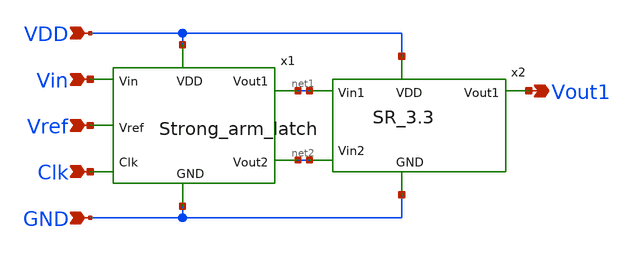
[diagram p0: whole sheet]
** sch_path: Comparator_Strong.sch
**.subckt Comparator_Strong Vin Vref Clk GND VDD Vout1
*.ipin Vin
*.ipin Vref
*.ipin Clk
*.ipin GND
*.ipin VDD
*.opin Vout1
x1 VDD net2 net1 Vin Vref Clk GND Strong_arm_latch
x2 net2 net1 VDD GND Vout1 SR_3.3
**.ends

* expanding   symbol:  /home/huydq/Strong_arm_latch.sym # of pins=7
** sym_path: Strong_arm_latch.sym
** sch_path: Strong_arm_latch.sch
.subckt Strong_arm_latch VDD Vout2 Vout1 Vin Vref Clk GND
*.ipin Vin
*.ipin Vref
*.ipin Clk
*.ipin VDD
*.opin Vout2
*.opin Vout1
*.ipin GND
XM8 Vout2 Vout1 net2 GND sky130_fd_pr__nfet_g5v0d10v5 L=0.5 W=8 nf=4 ad='int((nf+1)/2) * W/nf * 0.29'
+ as='int((nf+2)/2) * W/nf * 0.29' pd='2*int((nf+1)/2) * (W/nf + 0.29)' ps='2*int((nf+2)/2) * (W/nf + 0.29)'
+ nrd='0.29 / W' nrs='0.29 / W' sa=0 sb=0 sd=0 mult=1 m=1
XM7 Vout1 Vout2 net1 GND sky130_fd_pr__nfet_g5v0d10v5 L=0.5 W=8 nf=4 ad='int((nf+1)/2) * W/nf * 0.29'
+ as='int((nf+2)/2) * W/nf * 0.29' pd='2*int((nf+1)/2) * (W/nf + 0.29)' ps='2*int((nf+2)/2) * (W/nf + 0.29)'
+ nrd='0.29 / W' nrs='0.29 / W' sa=0 sb=0 sd=0 mult=1 m=1
XM10 Vout2 Vout1 VDD VDD sky130_fd_pr__pfet_g5v0d10v5 L=0.5 W=16 nf=8 ad='int((nf+1)/2) * W/nf * 0.29'
+ as='int((nf+2)/2) * W/nf * 0.29' pd='2*int((nf+1)/2) * (W/nf + 0.29)' ps='2*int((nf+2)/2) * (W/nf + 0.29)'
+ nrd='0.29 / W' nrs='0.29 / W' sa=0 sb=0 sd=0 mult=1 m=1
XM1 Vout1 Vout2 VDD VDD sky130_fd_pr__pfet_g5v0d10v5 L=0.5 W=16 nf=8 ad='int((nf+1)/2) * W/nf * 0.29'
+ as='int((nf+2)/2) * W/nf * 0.29' pd='2*int((nf+1)/2) * (W/nf + 0.29)' ps='2*int((nf+2)/2) * (W/nf + 0.29)'
+ nrd='0.29 / W' nrs='0.29 / W' sa=0 sb=0 sd=0 mult=1 m=1
XM2 net1 Clk VDD VDD sky130_fd_pr__pfet_g5v0d10v5 L=0.5 W=2 nf=2 ad='int((nf+1)/2) * W/nf * 0.29' as='int((nf+2)/2) * W/nf * 0.29'
+ pd='2*int((nf+1)/2) * (W/nf + 0.29)' ps='2*int((nf+2)/2) * (W/nf + 0.29)' nrd='0.29 / W' nrs='0.29 / W'
+ sa=0 sb=0 sd=0 mult=1 m=1
XM3 Vout1 Clk VDD VDD sky130_fd_pr__pfet_g5v0d10v5 L=0.5 W=2 nf=2 ad='int((nf+1)/2) * W/nf * 0.29' as='int((nf+2)/2) * W/nf * 0.29'
+ pd='2*int((nf+1)/2) * (W/nf + 0.29)' ps='2*int((nf+2)/2) * (W/nf + 0.29)' nrd='0.29 / W' nrs='0.29 / W'
+ sa=0 sb=0 sd=0 mult=1 m=1
XM4 Vout2 Clk VDD VDD sky130_fd_pr__pfet_g5v0d10v5 L=0.5 W=2 nf=2 ad='int((nf+1)/2) * W/nf * 0.29' as='int((nf+2)/2) * W/nf * 0.29'
+ pd='2*int((nf+1)/2) * (W/nf + 0.29)' ps='2*int((nf+2)/2) * (W/nf + 0.29)' nrd='0.29 / W' nrs='0.29 / W'
+ sa=0 sb=0 sd=0 mult=1 m=1
XM5 net2 Clk VDD VDD sky130_fd_pr__pfet_g5v0d10v5 L=0.5 W=2 nf=2 ad='int((nf+1)/2) * W/nf * 0.29' as='int((nf+2)/2) * W/nf * 0.29'
+ pd='2*int((nf+1)/2) * (W/nf + 0.29)' ps='2*int((nf+2)/2) * (W/nf + 0.29)' nrd='0.29 / W' nrs='0.29 / W'
+ sa=0 sb=0 sd=0 mult=1 m=1
XM6 net1 Vop GND GND sky130_fd_pr__nfet_g5v0d10v5 L=0.5 W=12 nf=6 ad='int((nf+1)/2) * W/nf * 0.29' as='int((nf+2)/2) * W/nf * 0.29'
+ pd='2*int((nf+1)/2) * (W/nf + 0.29)' ps='2*int((nf+2)/2) * (W/nf + 0.29)' nrd='0.29 / W' nrs='0.29 / W'
+ sa=0 sb=0 sd=0 mult=1 m=1
XM9 net2 Von GND GND sky130_fd_pr__nfet_g5v0d10v5 L=0.5 W=12 nf=6 ad='int((nf+1)/2) * W/nf * 0.29' as='int((nf+2)/2) * W/nf * 0.29'
+ pd='2*int((nf+1)/2) * (W/nf + 0.29)' ps='2*int((nf+2)/2) * (W/nf + 0.29)' nrd='0.29 / W' nrs='0.29 / W'
+ sa=0 sb=0 sd=0 mult=1 m=1
XM16 net3 Clk_not VDD VDD sky130_fd_pr__pfet_g5v0d10v5 L=1 W=10 nf=4 ad='int((nf+1)/2) * W/nf * 0.29'
+ as='int((nf+2)/2) * W/nf * 0.29' pd='2*int((nf+1)/2) * (W/nf + 0.29)' ps='2*int((nf+2)/2) * (W/nf + 0.29)'
+ nrd='0.29 / W' nrs='0.29 / W' sa=0 sb=0 sd=0 mult=1 m=1
XM17 Vop Vin net3 VDD sky130_fd_pr__pfet_g5v0d10v5 L=1 W=40 nf=20 ad='int((nf+1)/2) * W/nf * 0.29' as='int((nf+2)/2) * W/nf * 0.29'
+ pd='2*int((nf+1)/2) * (W/nf + 0.29)' ps='2*int((nf+2)/2) * (W/nf + 0.29)' nrd='0.29 / W' nrs='0.29 / W'
+ sa=0 sb=0 sd=0 mult=1 m=1
XM18 Von Vref net3 VDD sky130_fd_pr__pfet_g5v0d10v5 L=1 W=40 nf=20 ad='int((nf+1)/2) * W/nf * 0.29' as='int((nf+2)/2) * W/nf * 0.29'
+ pd='2*int((nf+1)/2) * (W/nf + 0.29)' ps='2*int((nf+2)/2) * (W/nf + 0.29)' nrd='0.29 / W' nrs='0.29 / W'
+ sa=0 sb=0 sd=0 mult=1 m=1
XM19 Vop Clk_not GND GND sky130_fd_pr__nfet_g5v0d10v5 L=0.5 W=2 nf=1 ad='int((nf+1)/2) * W/nf * 0.29'
+ as='int((nf+2)/2) * W/nf * 0.29' pd='2*int((nf+1)/2) * (W/nf + 0.29)' ps='2*int((nf+2)/2) * (W/nf + 0.29)'
+ nrd='0.29 / W' nrs='0.29 / W' sa=0 sb=0 sd=0 mult=1 m=1
XM20 Von Clk_not GND GND sky130_fd_pr__nfet_g5v0d10v5 L=0.5 W=2 nf=1 ad='int((nf+1)/2) * W/nf * 0.29'
+ as='int((nf+2)/2) * W/nf * 0.29' pd='2*int((nf+1)/2) * (W/nf + 0.29)' ps='2*int((nf+2)/2) * (W/nf + 0.29)'
+ nrd='0.29 / W' nrs='0.29 / W' sa=0 sb=0 sd=0 mult=1 m=1
XM11 Clk_not Clk GND GND sky130_fd_pr__nfet_g5v0d10v5 L=0.5 W=4 nf=2 ad='int((nf+1)/2) * W/nf * 0.29'
+ as='int((nf+2)/2) * W/nf * 0.29' pd='2*int((nf+1)/2) * (W/nf + 0.29)' ps='2*int((nf+2)/2) * (W/nf + 0.29)'
+ nrd='0.29 / W' nrs='0.29 / W' sa=0 sb=0 sd=0 mult=1 m=1
XM13 Clk_not Clk VDD VDD sky130_fd_pr__pfet_g5v0d10v5 L=0.5 W=10 nf=4 ad='int((nf+1)/2) * W/nf * 0.29'
+ as='int((nf+2)/2) * W/nf * 0.29' pd='2*int((nf+1)/2) * (W/nf + 0.29)' ps='2*int((nf+2)/2) * (W/nf + 0.29)'
+ nrd='0.29 / W' nrs='0.29 / W' sa=0 sb=0 sd=0 mult=1 m=1
.ends


* expanding   symbol:  /home/huydq/SR_3.3.sym # of pins=5
** sym_path: SR_3.3.sym
** sch_path: SR_3.3.sch
.subckt SR_3.3 Vin2 Vin1 VDD GND Vout1
*.ipin Vin1
*.ipin Vin2
*.ipin VDD
*.ipin GND
*.opin Vout1
XM9 net3 Vin1 GND GND sky130_fd_pr__nfet_g5v0d10v5 L=0.5 W=4 nf=2 ad='int((nf+1)/2) * W/nf * 0.29' as='int((nf+2)/2) * W/nf * 0.29'
+ pd='2*int((nf+1)/2) * (W/nf + 0.29)' ps='2*int((nf+2)/2) * (W/nf + 0.29)' nrd='0.29 / W' nrs='0.29 / W'
+ sa=0 sb=0 sd=0 mult=1 m=1
XM1 Vo1 net3 GND GND sky130_fd_pr__nfet_g5v0d10v5 L=0.5 W=4 nf=2 ad='int((nf+1)/2) * W/nf * 0.29' as='int((nf+2)/2) * W/nf * 0.29'
+ pd='2*int((nf+1)/2) * (W/nf + 0.29)' ps='2*int((nf+2)/2) * (W/nf + 0.29)' nrd='0.29 / W' nrs='0.29 / W'
+ sa=0 sb=0 sd=0 mult=1 m=1
XM2 net1 net2 GND GND sky130_fd_pr__nfet_g5v0d10v5 L=0.5 W=4 nf=2 ad='int((nf+1)/2) * W/nf * 0.29' as='int((nf+2)/2) * W/nf * 0.29'
+ pd='2*int((nf+1)/2) * (W/nf + 0.29)' ps='2*int((nf+2)/2) * (W/nf + 0.29)' nrd='0.29 / W' nrs='0.29 / W'
+ sa=0 sb=0 sd=0 mult=1 m=1
XM3 net2 Vin2 GND GND sky130_fd_pr__nfet_g5v0d10v5 L=0.5 W=4 nf=2 ad='int((nf+1)/2) * W/nf * 0.29' as='int((nf+2)/2) * W/nf * 0.29'
+ pd='2*int((nf+1)/2) * (W/nf + 0.29)' ps='2*int((nf+2)/2) * (W/nf + 0.29)' nrd='0.29 / W' nrs='0.29 / W'
+ sa=0 sb=0 sd=0 mult=1 m=1
XM4 net3 Vin1 VDD VDD sky130_fd_pr__pfet_g5v0d10v5 L=0.5 W=8 nf=4 ad='int((nf+1)/2) * W/nf * 0.29' as='int((nf+2)/2) * W/nf * 0.29'
+ pd='2*int((nf+1)/2) * (W/nf + 0.29)' ps='2*int((nf+2)/2) * (W/nf + 0.29)' nrd='0.29 / W' nrs='0.29 / W'
+ sa=0 sb=0 sd=0 mult=1 m=1
XM5 net1 Vo1 VDD VDD sky130_fd_pr__pfet_g5v0d10v5 L=0.5 W=8 nf=4 ad='int((nf+1)/2) * W/nf * 0.29' as='int((nf+2)/2) * W/nf * 0.29'
+ pd='2*int((nf+1)/2) * (W/nf + 0.29)' ps='2*int((nf+2)/2) * (W/nf + 0.29)' nrd='0.29 / W' nrs='0.29 / W'
+ sa=0 sb=0 sd=0 mult=1 m=1
XM6 Vo1 net1 VDD VDD sky130_fd_pr__pfet_g5v0d10v5 L=0.5 W=8 nf=4 ad='int((nf+1)/2) * W/nf * 0.29' as='int((nf+2)/2) * W/nf * 0.29'
+ pd='2*int((nf+1)/2) * (W/nf + 0.29)' ps='2*int((nf+2)/2) * (W/nf + 0.29)' nrd='0.29 / W' nrs='0.29 / W'
+ sa=0 sb=0 sd=0 mult=1 m=1
XM7 net2 Vin2 VDD VDD sky130_fd_pr__pfet_g5v0d10v5 L=0.5 W=8 nf=4 ad='int((nf+1)/2) * W/nf * 0.29' as='int((nf+2)/2) * W/nf * 0.29'
+ pd='2*int((nf+1)/2) * (W/nf + 0.29)' ps='2*int((nf+2)/2) * (W/nf + 0.29)' nrd='0.29 / W' nrs='0.29 / W'
+ sa=0 sb=0 sd=0 mult=1 m=1
XM8 Vout1 net4 GND GND sky130_fd_pr__nfet_g5v0d10v5 L=0.5 W=8 nf=4 ad='int((nf+1)/2) * W/nf * 0.29' as='int((nf+2)/2) * W/nf * 0.29'
+ pd='2*int((nf+1)/2) * (W/nf + 0.29)' ps='2*int((nf+2)/2) * (W/nf + 0.29)' nrd='0.29 / W' nrs='0.29 / W'
+ sa=0 sb=0 sd=0 mult=1 m=1
XM10 Vout1 net4 VDD VDD sky130_fd_pr__pfet_g5v0d10v5 L=0.5 W=16 nf=8 ad='int((nf+1)/2) * W/nf * 0.29'
+ as='int((nf+2)/2) * W/nf * 0.29' pd='2*int((nf+1)/2) * (W/nf + 0.29)' ps='2*int((nf+2)/2) * (W/nf + 0.29)'
+ nrd='0.29 / W' nrs='0.29 / W' sa=0 sb=0 sd=0 mult=1 m=1
XM11 net4 Vo1 GND GND sky130_fd_pr__nfet_g5v0d10v5 L=0.5 W=2 nf=1 ad='int((nf+1)/2) * W/nf * 0.29' as='int((nf+2)/2) * W/nf * 0.29'
+ pd='2*int((nf+1)/2) * (W/nf + 0.29)' ps='2*int((nf+2)/2) * (W/nf + 0.29)' nrd='0.29 / W' nrs='0.29 / W'
+ sa=0 sb=0 sd=0 mult=1 m=1
XM12 net4 Vo1 VDD VDD sky130_fd_pr__pfet_g5v0d10v5 L=0.5 W=4 nf=2 ad='int((nf+1)/2) * W/nf * 0.29' as='int((nf+2)/2) * W/nf * 0.29'
+ pd='2*int((nf+1)/2) * (W/nf + 0.29)' ps='2*int((nf+2)/2) * (W/nf + 0.29)' nrd='0.29 / W' nrs='0.29 / W'
+ sa=0 sb=0 sd=0 mult=1 m=1
.ends

.end
